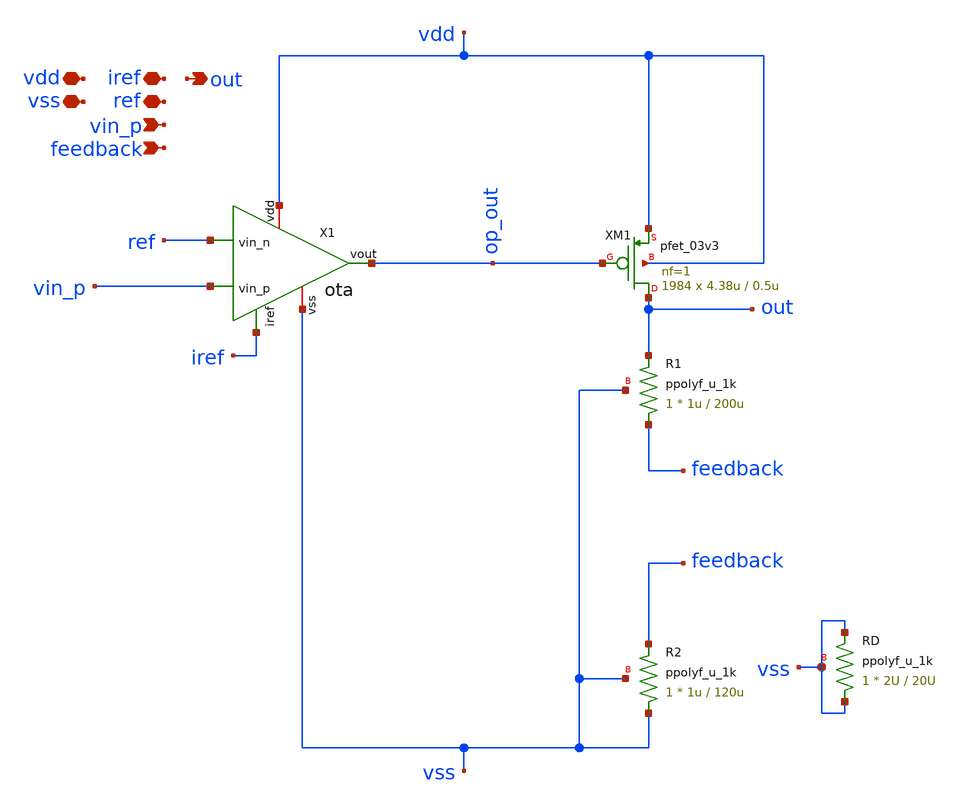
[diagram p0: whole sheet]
** sch_path: LDO/xschem/TOP_CHILE_OPEN_LDO/symbol/TOP_CHILE_OPEN_LDO.sch
**.subckt TOP_CHILE_OPEN_LDO ref iref vss vdd vin_p feedback out
*.iopin ref
*.iopin iref
*.iopin vss
*.iopin vdd
*.ipin vin_p
*.ipin feedback
*.opin out
X1 vdd iref ref vin_p op_out vss ota
XM1 out op_out vdd vdd pfet_03v3 L=0.5u W=4.38u nf=1 ad='int((nf+1)/2) * W/nf * 0.18u' as='int((nf+2)/2) * W/nf * 0.18u'
+ pd='2*int((nf+1)/2) * (W/nf + 0.18u)' ps='2*int((nf+2)/2) * (W/nf + 0.18u)' nrd='0.18u / W' nrs='0.18u / W'
+ sa=0 sb=0 sd=0 m=1984
XR1 feedback out vss ppolyf_u_1k r_width=1u r_length=200u m=1
XR2 vss feedback vss ppolyf_u_1k r_width=1u r_length=120u m=1
XRD vss vss vss ppolyf_u_1k r_width=2U r_length=20U m=1
**.ends
.end
